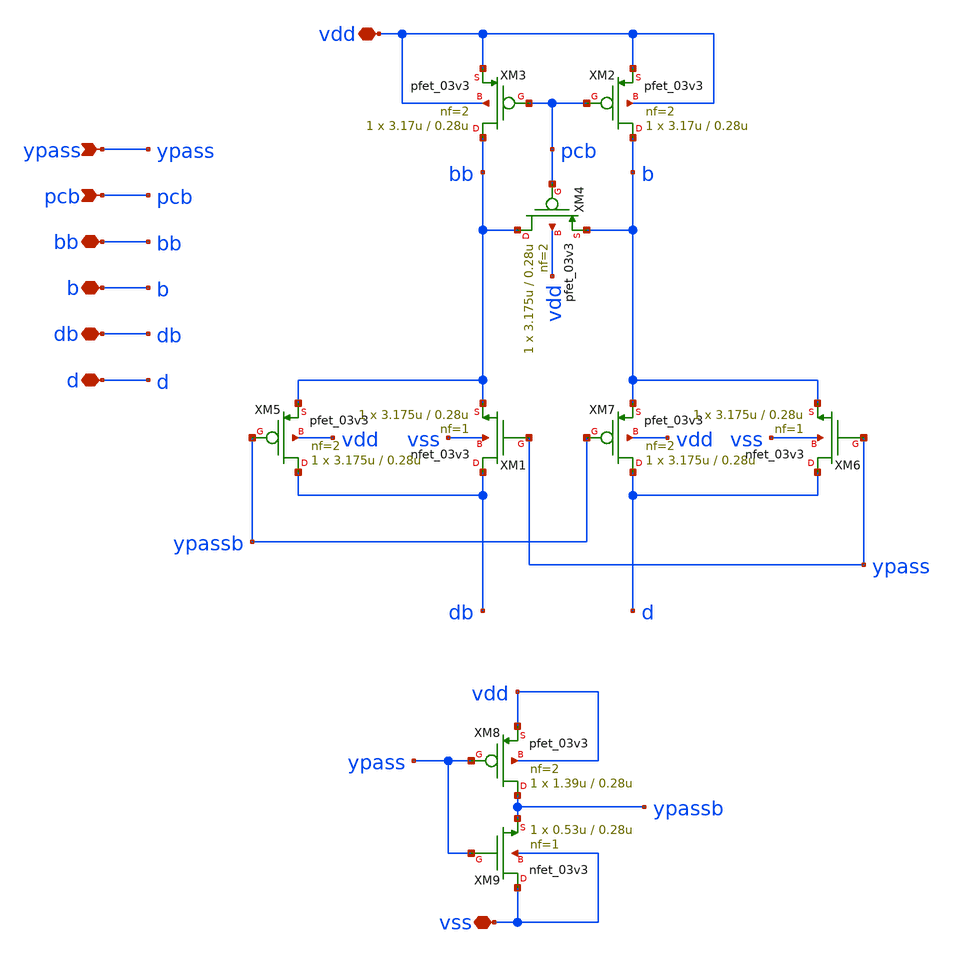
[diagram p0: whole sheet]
** sch_path: cells/gf180mcu_ocd_ip_sram__sram512x8m8wm1/xschem/ypass_gate_3v512x8m81.sch
**.subckt ypass_gate_3v512x8m81 vdd pcb bb b db d ypass vss
*.iopin vdd
*.ipin pcb
*.iopin bb
*.iopin b
*.iopin db
*.iopin d
*.ipin ypass
*.iopin vss
XM1 db ypass bb vss nfet_03v3 L=0.28u W=3.175u nf=1 ad='int((nf+1)/2) * W/nf * 0.18u' as='int((nf+2)/2) * W/nf * 0.18u'
+ pd='2*int((nf+1)/2) * (W/nf + 0.18u)' ps='2*int((nf+2)/2) * (W/nf + 0.18u)' nrd='0.18u / W' nrs='0.18u / W'
+ sa=0 sb=0 sd=0 m=1
XM3 bb pcb vdd vdd pfet_03v3 L=0.28u W=3.17u nf=2 ad='int((nf+1)/2) * W/nf * 0.18u' as='int((nf+2)/2) * W/nf * 0.18u'
+ pd='2*int((nf+1)/2) * (W/nf + 0.18u)' ps='2*int((nf+2)/2) * (W/nf + 0.18u)' nrd='0.18u / W' nrs='0.18u / W'
+ sa=0 sb=0 sd=0 m=1
XM2 b pcb vdd vdd pfet_03v3 L=0.28u W=3.17u nf=2 ad='int((nf+1)/2) * W/nf * 0.18u' as='int((nf+2)/2) * W/nf * 0.18u'
+ pd='2*int((nf+1)/2) * (W/nf + 0.18u)' ps='2*int((nf+2)/2) * (W/nf + 0.18u)' nrd='0.18u / W' nrs='0.18u / W'
+ sa=0 sb=0 sd=0 m=1
XM4 bb pcb b vdd pfet_03v3 L=0.28u W=3.175u nf=2 ad='int((nf+1)/2) * W/nf * 0.18u' as='int((nf+2)/2) * W/nf * 0.18u'
+ pd='2*int((nf+1)/2) * (W/nf + 0.18u)' ps='2*int((nf+2)/2) * (W/nf + 0.18u)' nrd='0.18u / W' nrs='0.18u / W'
+ sa=0 sb=0 sd=0 m=1
XM5 db ypassb bb vdd pfet_03v3 L=0.28u W=3.175u nf=2 ad='int((nf+1)/2) * W/nf * 0.18u' as='int((nf+2)/2) * W/nf * 0.18u'
+ pd='2*int((nf+1)/2) * (W/nf + 0.18u)' ps='2*int((nf+2)/2) * (W/nf + 0.18u)' nrd='0.18u / W' nrs='0.18u / W'
+ sa=0 sb=0 sd=0 m=1
XM7 d ypassb b vdd pfet_03v3 L=0.28u W=3.175u nf=2 ad='int((nf+1)/2) * W/nf * 0.18u' as='int((nf+2)/2) * W/nf * 0.18u'
+ pd='2*int((nf+1)/2) * (W/nf + 0.18u)' ps='2*int((nf+2)/2) * (W/nf + 0.18u)' nrd='0.18u / W' nrs='0.18u / W'
+ sa=0 sb=0 sd=0 m=1
XM6 d ypass b vss nfet_03v3 L=0.28u W=3.175u nf=1 ad='int((nf+1)/2) * W/nf * 0.18u' as='int((nf+2)/2) * W/nf * 0.18u'
+ pd='2*int((nf+1)/2) * (W/nf + 0.18u)' ps='2*int((nf+2)/2) * (W/nf + 0.18u)' nrd='0.18u / W' nrs='0.18u / W'
+ sa=0 sb=0 sd=0 m=1
XM8 ypassb ypass vdd vdd pfet_03v3 L=0.28u W=1.39u nf=2 ad='int((nf+1)/2) * W/nf * 0.18u' as='int((nf+2)/2) * W/nf * 0.18u'
+ pd='2*int((nf+1)/2) * (W/nf + 0.18u)' ps='2*int((nf+2)/2) * (W/nf + 0.18u)' nrd='0.18u / W' nrs='0.18u / W'
+ sa=0 sb=0 sd=0 m=1
XM9 vss ypass ypassb vss nfet_03v3 L=0.28u W=0.53u nf=1 ad='int((nf+1)/2) * W/nf * 0.18u' as='int((nf+2)/2) * W/nf * 0.18u'
+ pd='2*int((nf+1)/2) * (W/nf + 0.18u)' ps='2*int((nf+2)/2) * (W/nf + 0.18u)' nrd='0.18u / W' nrs='0.18u / W'
+ sa=0 sb=0 sd=0 m=1
**.ends
.end
